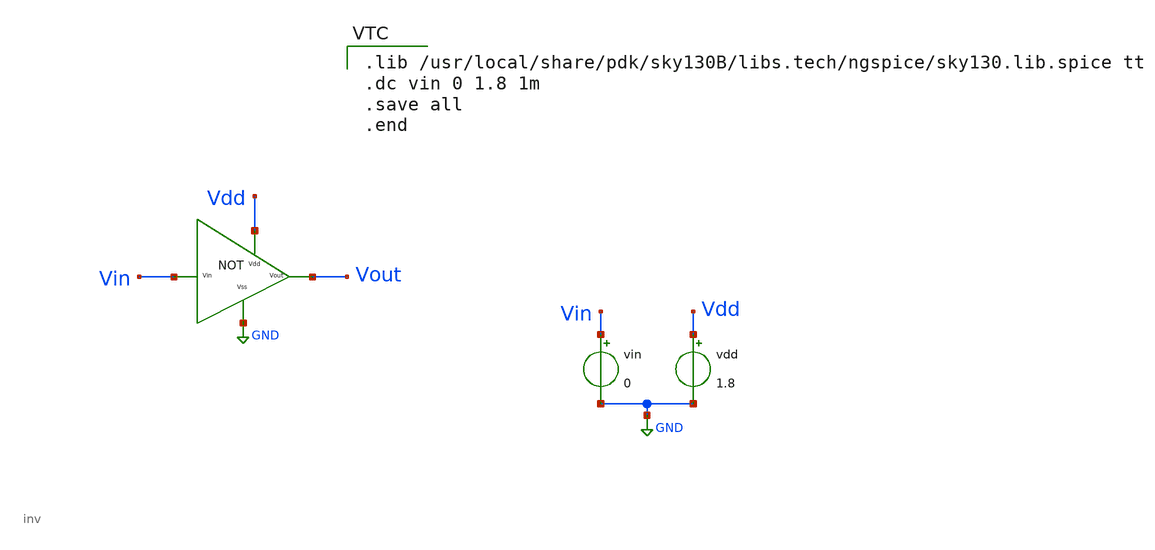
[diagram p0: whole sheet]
** sch_path: Xschem/inv_test.sch
**.subckt inv_test
x1 Vdd Vin Vout GND inv
vin Vin GND 0
vdd Vdd GND 1.8
**** begin user architecture code

.lib /usr/local/share/pdk/sky130B/libs.tech/ngspice/sky130.lib.spice tt
.dc vin 0 1.8 1m
.save all
.end

**** end user architecture code
**.ends

* expanding   symbol:  inv.sym # of pins=4
** sym_path: Xschem/inv.sym
** sch_path: Xschem/inv.sch
.subckt inv Vdd Vin Vout Vss
*.ipin Vin
*.ipin Vss
*.ipin Vdd
*.opin Vout
XM1 Vout Vin Vss GND sky130_fd_pr__nfet_01v8 L=0.15 W=1 nf=1 ad='int((nf+1)/2) * W/nf * 0.29' as='int((nf+2)/2) * W/nf * 0.29'
+ pd='2*int((nf+1)/2) * (W/nf + 0.29)' ps='2*int((nf+2)/2) * (W/nf + 0.29)' nrd='0.29 / W' nrs='0.29 / W'
+ sa=0 sb=0 sd=0 mult=1 m=1
XM2 Vout Vin Vdd VDD sky130_fd_pr__pfet_01v8 L=0.15 W=2.5 nf=1 ad='int((nf+1)/2) * W/nf * 0.29' as='int((nf+2)/2) * W/nf * 0.29'
+ pd='2*int((nf+1)/2) * (W/nf + 0.29)' ps='2*int((nf+2)/2) * (W/nf + 0.29)' nrd='0.29 / W' nrs='0.29 / W'
+ sa=0 sb=0 sd=0 mult=1 m=1
.ends

.GLOBAL GND
.end
